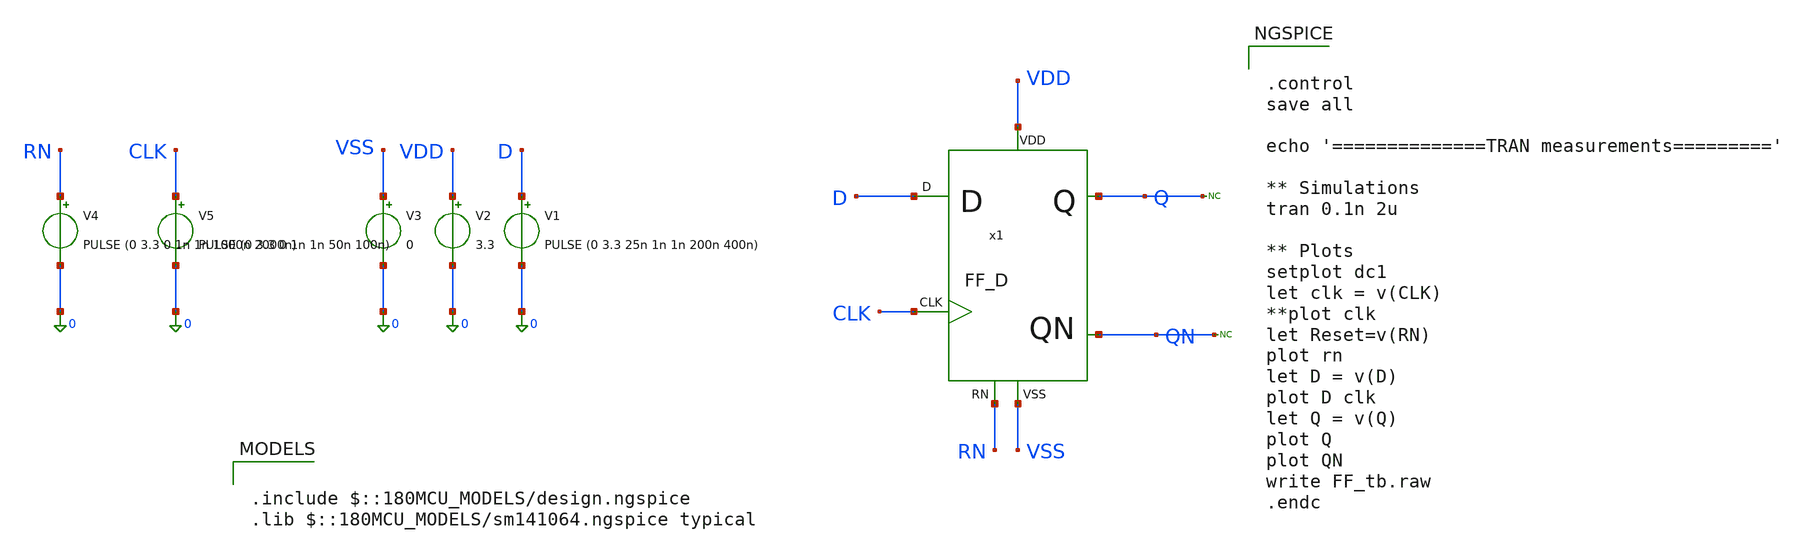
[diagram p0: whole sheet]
** sch_path: designs/sar_adc/digital/flip_flop/xschem/FF_tb.sch
**.subckt FF_tb
V1 D 0 PULSE (0 3.3 25n 1n 1n 200n 400n)
V2 VDD 0 3.3
V3 VSS 0 0
V5 CLK 0 PULSE (0 3.3 0 1n 1n 50n 100n)
x1 CLK D VDD VSS Q RN QN FF_D
V4 RN 0 PULSE (0 3.3 0 1n 1n 1000n 2000n)
* noconn Q
* noconn QN
**** begin user architecture code

.include $::180MCU_MODELS/design.ngspice
.lib $::180MCU_MODELS/sm141064.ngspice typical



.control
save all

echo '==============TRAN measurements========='

** Simulations
tran 0.1n 2u

** Plots
setplot dc1
let clk = v(CLK)
**plot clk
let Reset=v(RN)
plot rn
let D = v(D)
plot D clk
let Q = v(Q)
plot Q
plot QN
write FF_tb.raw
.endc


**** end user architecture code
**.ends

* expanding   symbol:  designs/sar_adc/digital/flip_flop/xschem/FF_D.sym # of pins=7
** sym_path: designs/sar_adc/digital/flip_flop/xschem/FF_D.sym
** sch_path: designs/sar_adc/digital/flip_flop/xschem/FF_D.sch
.subckt FF_D CLK D VDD VSS Q RN QN
*.iopin VDD
*.iopin VSS
*.iopin CLK
*.iopin D
*.iopin RN
*.iopin Q
*.iopin QN
x1 CLKN D VDD tg1 CLK VSS TG
x2 CLK2N net1 VDD net3 CLK2 VSS TG
x3 CLKN Q VDD net3 CLK VSS TG
x4 CLK2N net1 VDD tg1 CLK2 VSS TG
x5 VDD VSS RN tg1 nand1 NAND
x6 VDD VSS RN net3 net2 NAND
x8 VDD nand1 net1 VSS inverter
x9 VDD CLK CLK2 VSS inverter
x7 VDD net2 Q VSS inverter
x10 VDD CLK CLKN VSS inverter
x11 VDD CLK2 CLK2N VSS inverter
x12 VDD Q QN VSS inverter
.ends


* expanding   symbol:  designs/sar_adc/digital/TG/xschem/TG.sym # of pins=6
** sym_path: designs/sar_adc/digital/TG/xschem/TG.sym
** sch_path: designs/sar_adc/digital/TG/xschem/TG.sch
.subckt TG CLK A VDD B CLKN VSS
*.iopin VDD
*.iopin VSS
*.ipin CLK
*.ipin CLKN
*.iopin A
*.iopin B
XM1 A CLK B VSS nfet_03v3 L=0.28u W=0.22u nf=1 ad='int((nf+1)/2) * W/nf * 0.18u' as='int((nf+2)/2) * W/nf * 0.18u'
+ pd='2*int((nf+1)/2) * (W/nf + 0.18u)' ps='2*int((nf+2)/2) * (W/nf + 0.18u)' nrd='0.18u / W' nrs='0.18u / W'
+ sa=0 sb=0 sd=0 m=1
XM2 A CLKN B VDD pfet_03v3 L=0.28u W=0.22u nf=1 ad='int((nf+1)/2) * W/nf * 0.18u' as='int((nf+2)/2) * W/nf * 0.18u'
+ pd='2*int((nf+1)/2) * (W/nf + 0.18u)' ps='2*int((nf+2)/2) * (W/nf + 0.18u)' nrd='0.18u / W' nrs='0.18u / W'
+ sa=0 sb=0 sd=0 m=1
.ends


* expanding   symbol:  designs/sar_adc/digital/NAND/xschem/NAND.sym # of pins=5
** sym_path: designs/sar_adc/digital/NAND/xschem/NAND.sym
** sch_path: designs/sar_adc/digital/NAND/xschem/NAND.sch
.subckt NAND VDD VSS A B out
*.iopin VDD
*.iopin A
*.iopin B
*.iopin out
*.iopin VSS
xINVA VDD net1 net2 VSS inverter
xINVB[2] VDD net2 out VSS inverter
xINVB[1] VDD net2 out VSS inverter
xINVB[0] VDD net2 out VSS inverter
XM2 net1 A VDD VDD pfet_03v3 L=0.28u W=0.5u nf=1 ad='int((nf+1)/2) * W/nf * 0.18u' as='int((nf+2)/2) * W/nf * 0.18u'
+ pd='2*int((nf+1)/2) * (W/nf + 0.18u)' ps='2*int((nf+2)/2) * (W/nf + 0.18u)' nrd='0.18u / W' nrs='0.18u / W'
+ sa=0 sb=0 sd=0 m=2
XM1 net1 A net3 VSS nfet_03v3 L=0.28u W=0.5u nf=1 ad='int((nf+1)/2) * W/nf * 0.18u' as='int((nf+2)/2) * W/nf * 0.18u'
+ pd='2*int((nf+1)/2) * (W/nf + 0.18u)' ps='2*int((nf+2)/2) * (W/nf + 0.18u)' nrd='0.18u / W' nrs='0.18u / W'
+ sa=0 sb=0 sd=0 m=1
XM3 net1 B VDD VDD pfet_03v3 L=0.28u W=0.5u nf=1 ad='int((nf+1)/2) * W/nf * 0.18u' as='int((nf+2)/2) * W/nf * 0.18u'
+ pd='2*int((nf+1)/2) * (W/nf + 0.18u)' ps='2*int((nf+2)/2) * (W/nf + 0.18u)' nrd='0.18u / W' nrs='0.18u / W'
+ sa=0 sb=0 sd=0 m=2
XM4 net3 B VSS VSS nfet_03v3 L=0.28u W=0.5u nf=1 ad='int((nf+1)/2) * W/nf * 0.18u' as='int((nf+2)/2) * W/nf * 0.18u'
+ pd='2*int((nf+1)/2) * (W/nf + 0.18u)' ps='2*int((nf+2)/2) * (W/nf + 0.18u)' nrd='0.18u / W' nrs='0.18u / W'
+ sa=0 sb=0 sd=0 m=1
.ends


* expanding   symbol:  designs/sar_adc/digital/inverter/xschem/inverter.sym # of pins=6
** sym_path: designs/sar_adc/digital/inverter/xschem/inverter.sym
** sch_path: designs/sar_adc/digital/inverter/xschem/inverter.sch
.subckt inverter VDD in out VSS
*.opin out
*.iopin in
*.iopin VDD
*.iopin VSS
XM1 out in VSS VSS nfet_03v3 L=0.28u W=1u nf=1 ad='int((nf+1)/2) * W/nf * 0.18u' as='int((nf+2)/2) * W/nf * 0.18u'
+ pd='2*int((nf+1)/2) * (W/nf + 0.18u)' ps='2*int((nf+2)/2) * (W/nf + 0.18u)' nrd='0.18u / W' nrs='0.18u / W'
+ sa=0 sb=0 sd=0 m=1
XM2 out in VDD VDD pfet_03v3 L=0.28u W=3u nf=1 ad='int((nf+1)/2) * W/nf * 0.18u' as='int((nf+2)/2) * W/nf * 0.18u'
+ pd='2*int((nf+1)/2) * (W/nf + 0.18u)' ps='2*int((nf+2)/2) * (W/nf + 0.18u)' nrd='0.18u / W' nrs='0.18u / W'
+ sa=0 sb=0 sd=0 m=1
.ends

.end
